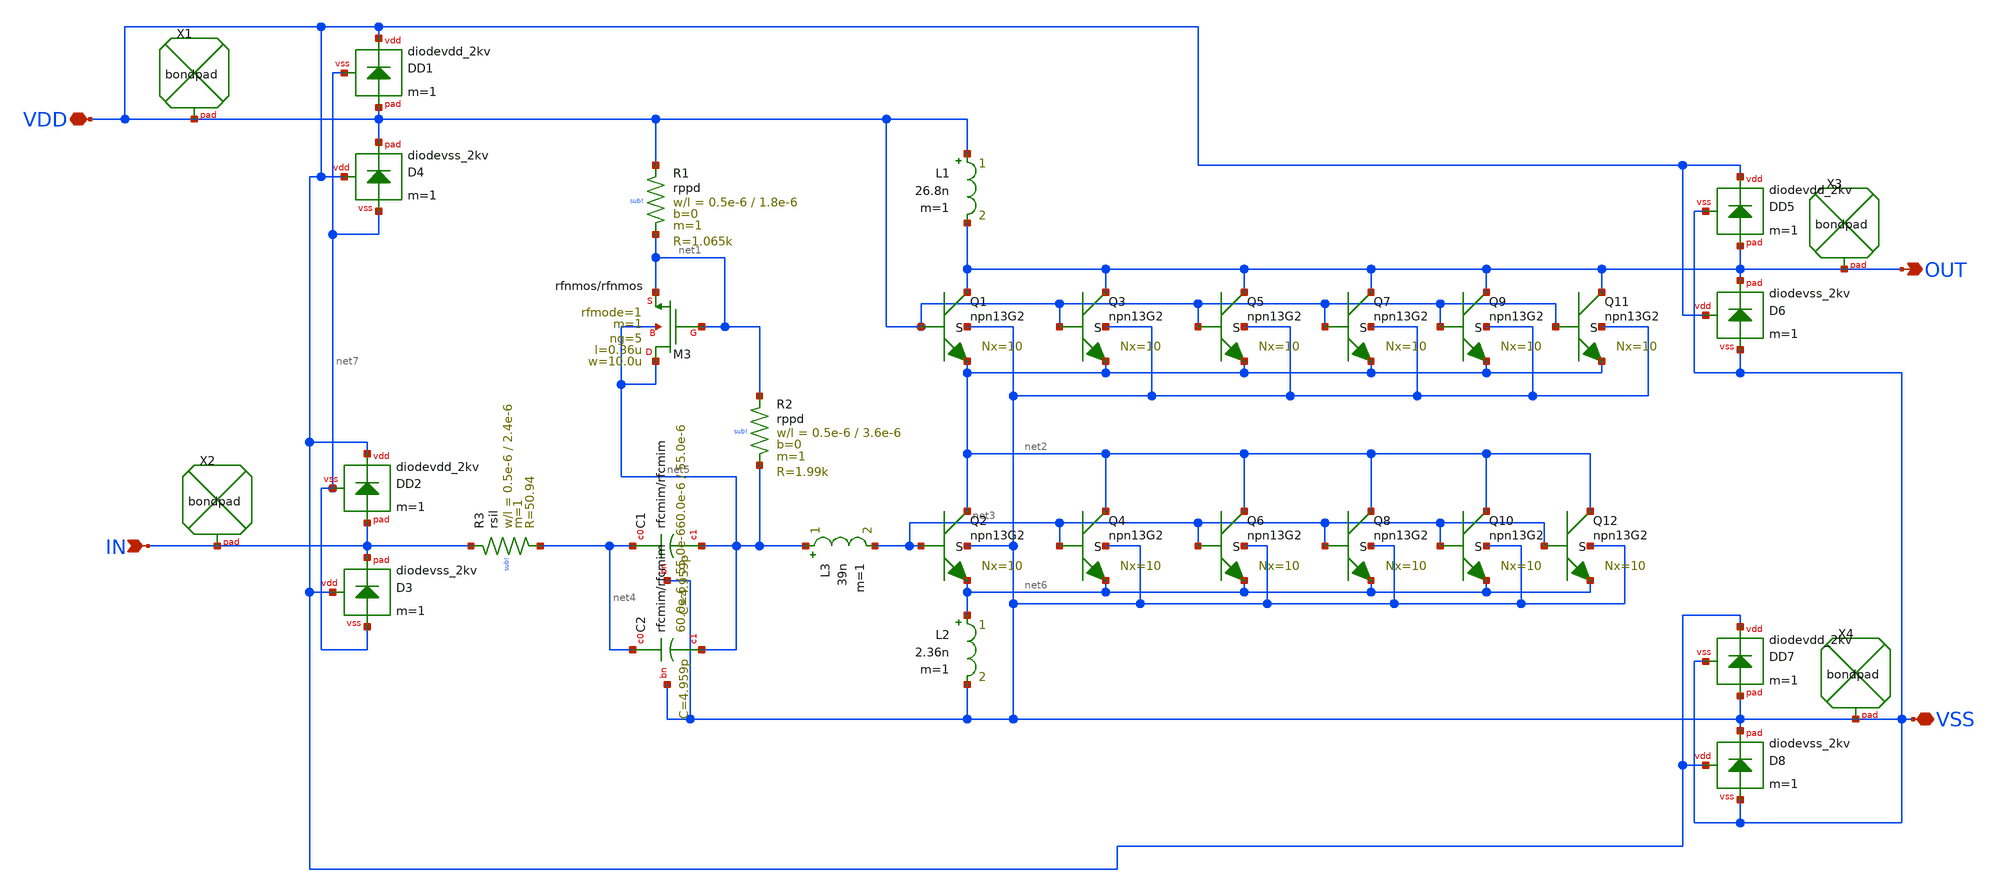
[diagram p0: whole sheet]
** sch_path: GPS_LNA/design_data/xschem/lna_full_pad.sch
**.subckt lna_full_pad VDD IN OUT VSS
*.iopin VDD
*.ipin IN
*.opin OUT
*.iopin VSS
XR2 net1 net5 sub! rppd w=0.5e-6 l=3.6e-6 m=1 b=0 mm_ok=1
XR1 VDD net1 sub! rppd w=0.5e-6 l=1.8e-6 m=1 b=0 mm_ok=1
XR3 IN net4 sub! rsil w=0.5e-6 l=2.4e-6 m=1 mm_ok=1
XC1 net4 net5 VSS rfcmim w=60.0e-6 l=55.0e-6 wfeed=5.0e-6 m=1 mm_ok=1
XC2 net4 net5 VSS rfcmim w=60.0e-6 l=55.0e-6 wfeed=5.0e-6 m=1 mm_ok=1
XM3 net5 net1 net1 net5 rfnmos w=10.0u l=0.36u ng=5 m=1 rfmode=1 mm_ok=1
XX1 VDD bondpad size=100u shape=0 padtype=0
XX3 OUT bondpad size=100u shape=0 padtype=0
XX4 VSS bondpad size=100u shape=0 padtype=0
XD1 VDD VDD net7 diodevdd_2kv m=1
XD4 VDD VDD net7 diodevss_2kv m=1
XX2 IN bondpad size=100u shape=0 padtype=0
XQ1 OUT VDD net2 VSS npn13G2 Nx=10 mm_ok=1
XQ2 net2 net3 net6 VSS npn13G2 Nx=10 mm_ok=1
XQ3 OUT VDD net2 VSS npn13G2 Nx=10 mm_ok=1
XQ4 net2 net3 net6 VSS npn13G2 Nx=10 mm_ok=1
XQ5 OUT VDD net2 VSS npn13G2 Nx=10 mm_ok=1
XQ6 net2 net3 net6 VSS npn13G2 Nx=10 mm_ok=1
XQ7 OUT VDD net2 VSS npn13G2 Nx=10 mm_ok=1
XQ8 net2 net3 net6 VSS npn13G2 Nx=10 mm_ok=1
XD2 VDD IN net7 diodevdd_2kv m=1
XD3 VDD IN net7 diodevss_2kv m=1
XD5 VDD OUT VSS diodevdd_2kv m=1
XD6 VDD OUT VSS diodevss_2kv m=1
XD7 VDD VSS VSS diodevdd_2kv m=1
XD8 VDD VSS VSS diodevss_2kv m=1
XQ9 OUT VDD net2 VSS npn13G2 Nx=10 mm_ok=1
XQ10 net2 net3 net6 VSS npn13G2 Nx=10 mm_ok=1
XQ11 OUT VDD net2 VSS npn13G2 Nx=10 mm_ok=1
XQ12 net2 net3 net6 VSS npn13G2 Nx=10 mm_ok=1
L1 VDD OUT 26.8n m=1
L2 net6 VSS 2.36n m=1
L3 net5 net3 39n m=1
**.ends
.end
